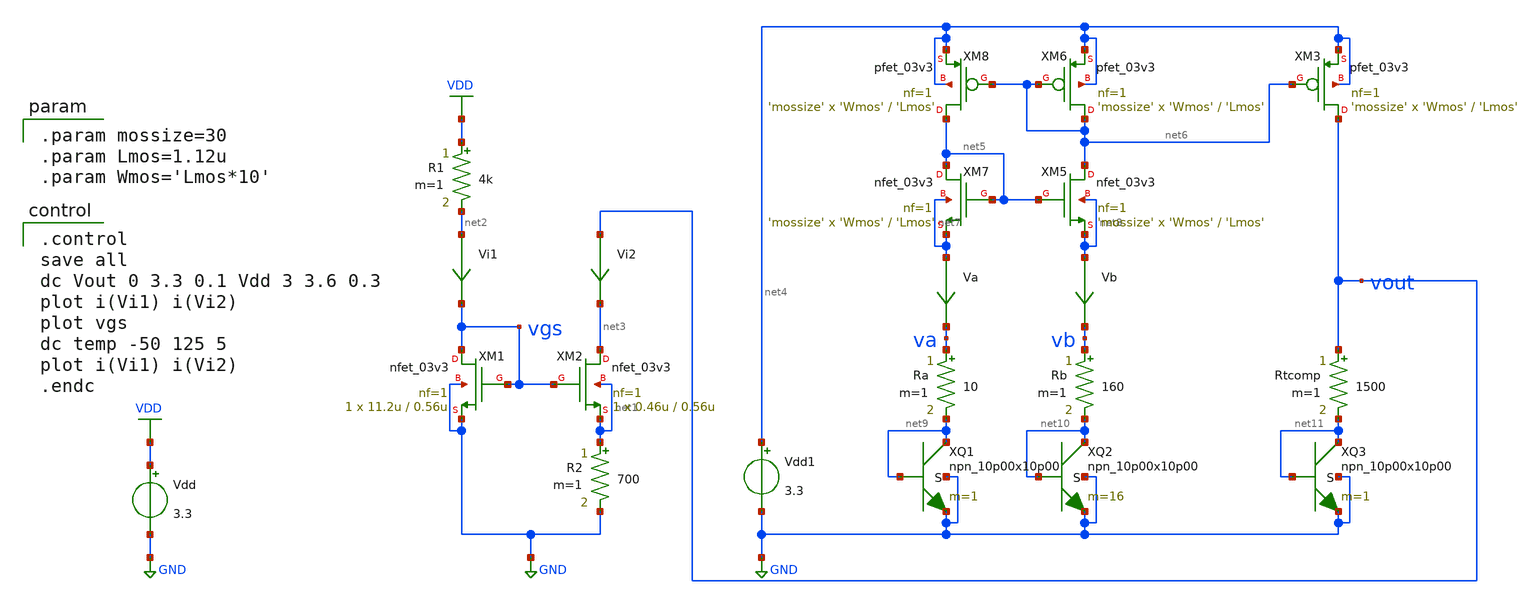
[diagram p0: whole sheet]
** sch_path: designs/cs-widlar.sch
**.subckt cs-widlar
Vdd VDD GND 3.3
XM1 vgs vgs GND GND nfet_03v3 L=0.56u W=11.2u nf=1 ad='int((nf+1)/2) * W/nf * 0.18u' as='int((nf+2)/2) * W/nf * 0.18u'
+ pd='2*int((nf+1)/2) * (W/nf + 0.18u)' ps='2*int((nf+2)/2) * (W/nf + 0.18u)' nrd='0.18u / W' nrs='0.18u / W'
+ sa=0 sb=0 sd=0 m=1
XM2 net3 vgs net1 net1 nfet_03v3 L=0.56u W=0.46u nf=1 ad='int((nf+1)/2) * W/nf * 0.18u' as='int((nf+2)/2) * W/nf * 0.18u'
+ pd='2*int((nf+1)/2) * (W/nf + 0.18u)' ps='2*int((nf+2)/2) * (W/nf + 0.18u)' nrd='0.18u / W' nrs='0.18u / W'
+ sa=0 sb=0 sd=0 m=1
Vi1 net2 vgs 0
.save i(vi1)
Vi2 vout net3 0
.save i(vi2)
R1 VDD net2 4k m=1
R2 net1 GND 700 m=1
XM5 net6 net5 net8 net8 nfet_03v3 L='Lmos' W='Wmos' nf=1 ad='int((nf+1)/2) * W/nf * 0.18u' as='int((nf+2)/2) * W/nf * 0.18u'
+ pd='2*int((nf+1)/2) * (W/nf + 0.18u)' ps='2*int((nf+2)/2) * (W/nf + 0.18u)' nrd='0.18u / W' nrs='0.18u / W'
+ sa=0 sb=0 sd=0 m='mossize'
XM6 net6 net6 net4 net4 pfet_03v3 L='Lmos' W='Wmos' nf=1 ad='int((nf+1)/2) * W/nf * 0.18u' as='int((nf+2)/2) * W/nf * 0.18u'
+ pd='2*int((nf+1)/2) * (W/nf + 0.18u)' ps='2*int((nf+2)/2) * (W/nf + 0.18u)' nrd='0.18u / W' nrs='0.18u / W'
+ sa=0 sb=0 sd=0 m='mossize'
XM7 net5 net5 net7 net7 nfet_03v3 L='Lmos' W='Wmos' nf=1 ad='int((nf+1)/2) * W/nf * 0.18u' as='int((nf+2)/2) * W/nf * 0.18u'
+ pd='2*int((nf+1)/2) * (W/nf + 0.18u)' ps='2*int((nf+2)/2) * (W/nf + 0.18u)' nrd='0.18u / W' nrs='0.18u / W'
+ sa=0 sb=0 sd=0 m='mossize'
XM8 net5 net6 net4 net4 pfet_03v3 L='Lmos' W='Wmos' nf=1 ad='int((nf+1)/2) * W/nf * 0.18u' as='int((nf+2)/2) * W/nf * 0.18u'
+ pd='2*int((nf+1)/2) * (W/nf + 0.18u)' ps='2*int((nf+2)/2) * (W/nf + 0.18u)' nrd='0.18u / W' nrs='0.18u / W'
+ sa=0 sb=0 sd=0 m='mossize'
Vb net8 vb 0
.save i(vb)
Va net7 va 0
.save i(va)
XQ1 net9 net9 GND GND npn_10p00x10p00 m=1
XQ2 net10 net10 GND GND npn_10p00x10p00 m=16
Rb vb net10 160 m=1
Ra va net9 10 m=1
XM3 vout net6 net4 net4 pfet_03v3 L='Lmos' W='Wmos' nf=1 ad='int((nf+1)/2) * W/nf * 0.18u' as='int((nf+2)/2) * W/nf * 0.18u'
+ pd='2*int((nf+1)/2) * (W/nf + 0.18u)' ps='2*int((nf+2)/2) * (W/nf + 0.18u)' nrd='0.18u / W' nrs='0.18u / W'
+ sa=0 sb=0 sd=0 m='mossize'
XQ3 net11 net11 GND GND npn_10p00x10p00 m=1
Rtcomp vout net11 1500 m=1
Vdd1 net4 GND 3.3
**** begin user architecture code

.include $::180MCU_MODELS/design.ngspice
.lib $::180MCU_MODELS/sm141064.ngspice typical
.lib $::180MCU_MODELS/sm141064.ngspice res_typical
.lib $::180MCU_MODELS/sm141064.ngspice moscap_typical
.lib $::180MCU_MODELS/sm141064.ngspice bjt_typical
* .lib $::180MCU_MODELS/sm141064.ngspice res_statistical


.control
save all
dc Vout 0 3.3 0.1 Vdd 3 3.6 0.3
plot i(Vi1) i(Vi2)
plot vgs
dc temp -50 125 5
plot i(Vi1) i(Vi2)
.endc


.include $::180MCU_MODELS/design.ngspice
.lib $::180MCU_MODELS/sm141064.ngspice typical
.lib $::180MCU_MODELS/sm141064.ngspice res_typical
.lib $::180MCU_MODELS/sm141064.ngspice moscap_typical
.lib $::180MCU_MODELS/sm141064.ngspice bjt_typical
* .lib $::180MCU_MODELS/sm141064.ngspice res_statistical


.param mossize=30
.param Lmos=1.12u
.param Wmos='Lmos*10'

**** end user architecture code
**.ends
.GLOBAL GND
.GLOBAL VDD
.end
